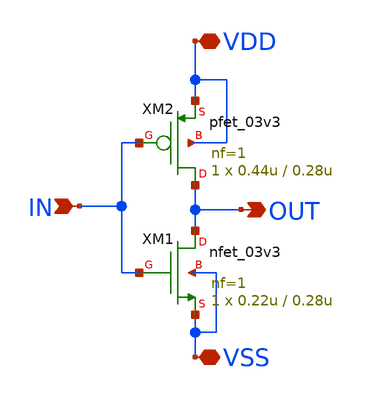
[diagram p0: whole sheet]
** sch_path: src/UN_PFD_GF180mcuD/UN_INV0_GF180mcuD.sch
**.subckt UN_INV0_GF180mcuD VDD VSS IN OUT
*.iopin VDD
*.iopin VSS
*.ipin IN
*.opin OUT
XM1 OUT IN VSS VSS nfet_03v3 L=0.28u W=0.22u nf=1 ad='int((nf+1)/2) * W/nf * 0.18u' as='int((nf+2)/2) * W/nf * 0.18u'
+ pd='2*int((nf+1)/2) * (W/nf + 0.18u)' ps='2*int((nf+2)/2) * (W/nf + 0.18u)' nrd='0.18u / W' nrs='0.18u / W'
+ sa=0 sb=0 sd=0 m=1
XM2 OUT IN VDD VDD pfet_03v3 L=0.28u W=0.44u nf=1 ad='int((nf+1)/2) * W/nf * 0.18u' as='int((nf+2)/2) * W/nf * 0.18u'
+ pd='2*int((nf+1)/2) * (W/nf + 0.18u)' ps='2*int((nf+2)/2) * (W/nf + 0.18u)' nrd='0.18u / W' nrs='0.18u / W'
+ sa=0 sb=0 sd=0 m=1
**.ends
.end
